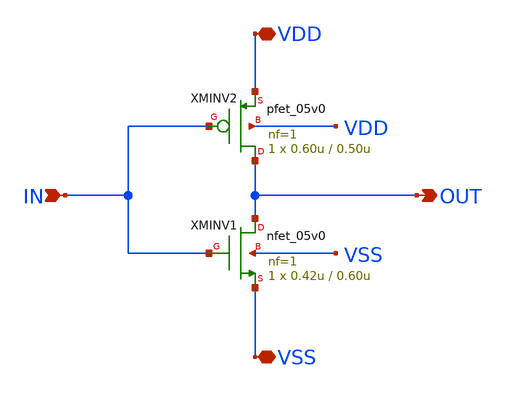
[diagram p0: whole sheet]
** sch_path: designs/libs/core_test/test_inv/test_inv.sch
**.subckt test_inv OUT IN VDD VSS
*.opin OUT
*.ipin IN
*.iopin VDD
*.iopin VSS
XMINV1 OUT IN VSS VSS nfet_05v0 L=0.60u W=0.42u nf=1 ad='int((nf+1)/2) * W/nf * 0.18u' as='int((nf+2)/2) * W/nf * 0.18u'
+ pd='2*int((nf+1)/2) * (W/nf + 0.18u)' ps='2*int((nf+2)/2) * (W/nf + 0.18u)' nrd='0.18u / W' nrs='0.18u / W'
+ sa=0 sb=0 sd=0 m=1
XMINV2 OUT IN VDD VDD pfet_05v0 L=0.50u W=0.60u nf=1 ad='int((nf+1)/2) * W/nf * 0.18u' as='int((nf+2)/2) * W/nf * 0.18u'
+ pd='2*int((nf+1)/2) * (W/nf + 0.18u)' ps='2*int((nf+2)/2) * (W/nf + 0.18u)' nrd='0.18u / W' nrs='0.18u / W'
+ sa=0 sb=0 sd=0 m=1
**.ends
.end
